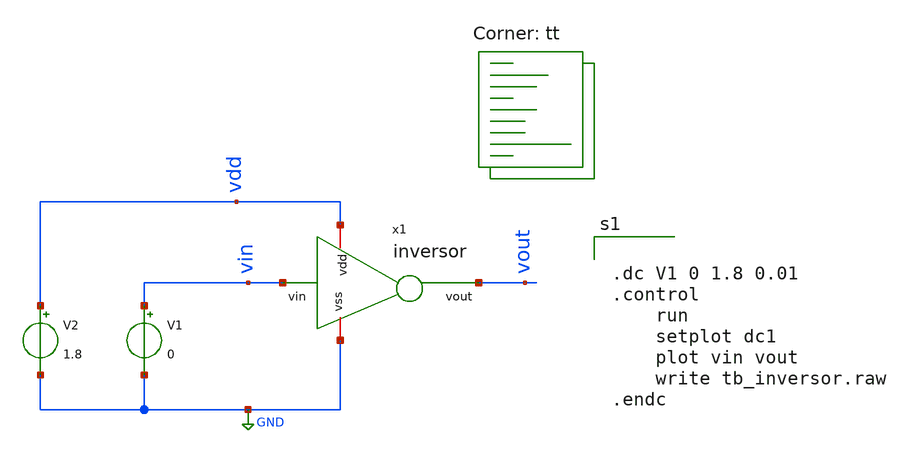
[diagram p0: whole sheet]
** sch_path: DIA2/tb_inversor.sch
**.subckt tb_inversor
x1 vdd vin vout GND inversor
V1 vin GND 0
V2 vdd GND 1.8
**** begin user architecture code
.lib $::SKYWATER_MODELS/sky130.lib.spice tt


.dc V1 0 1.8 0.01
.control
	run
	setplot dc1
	plot vin vout
	write tb_inversor.raw
.endc


**** end user architecture code
**.ends

* expanding   symbol:  /foss/designs/curso2025/inversor.sym # of pins=4
** sym_path: DIA2/inversor.sym
** sch_path: DIA2/inversor.sch
.subckt inversor vdd vin vout vss
*.ipin vin
*.opin vout
*.iopin vdd
*.iopin vss
XM11 vout vin vdd vdd sky130_fd_pr__pfet_01v8 L=0.15 W=3 nf=1 ad='int((nf+1)/2) * W/nf * 0.29' as='int((nf+2)/2) * W/nf * 0.29'
+ pd='2*int((nf+1)/2) * (W/nf + 0.29)' ps='2*int((nf+2)/2) * (W/nf + 0.29)' nrd='0.29 / W' nrs='0.29 / W'
+ sa=0 sb=0 sd=0 mult=1 m=1
XM2 vout vin vss vss sky130_fd_pr__nfet_01v8 L=0.15 W=1.5 nf=1 ad='int((1 + 1)/2) * 1.5 / 1 * 0.29' as='int((1 + 2)/2) * 1.5 / 1 * 0.29'
+ pd='2*int((1 + 1)/2) * (1.5 / 1 + 0.29)' ps='2*int((1 + 2)/2) * (1.5 / 1 + 0.29)' nrd='0.29 / 1.5 ' nrs='0.29 / 1.5 '
+ sa=0 sb=0 sd=0 mult=1 m=1
.ends

.GLOBAL GND
.end
